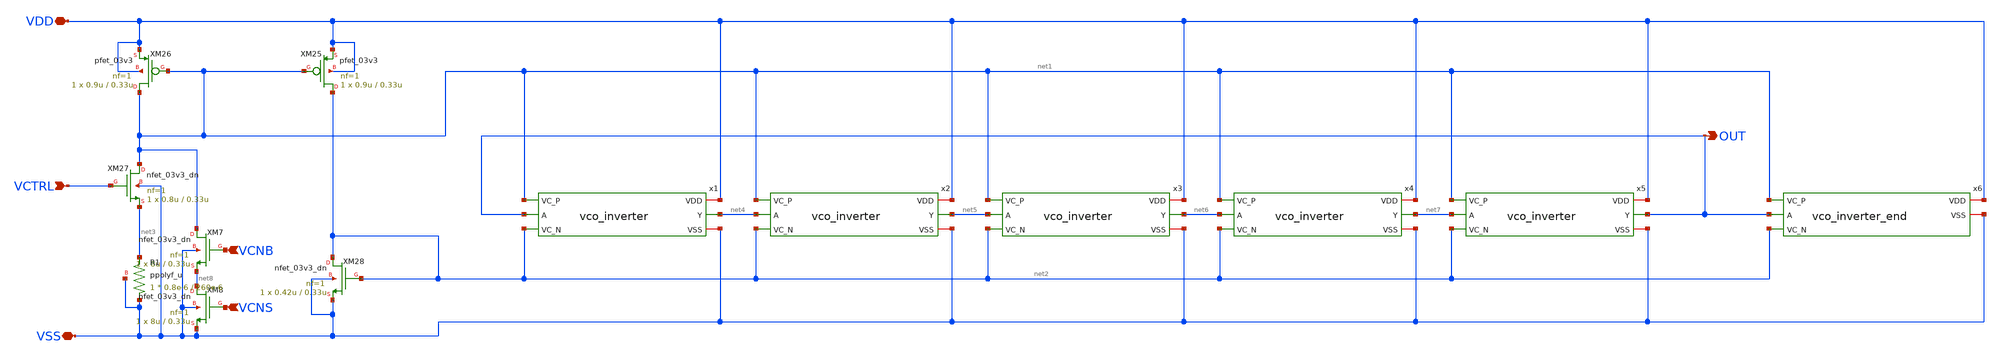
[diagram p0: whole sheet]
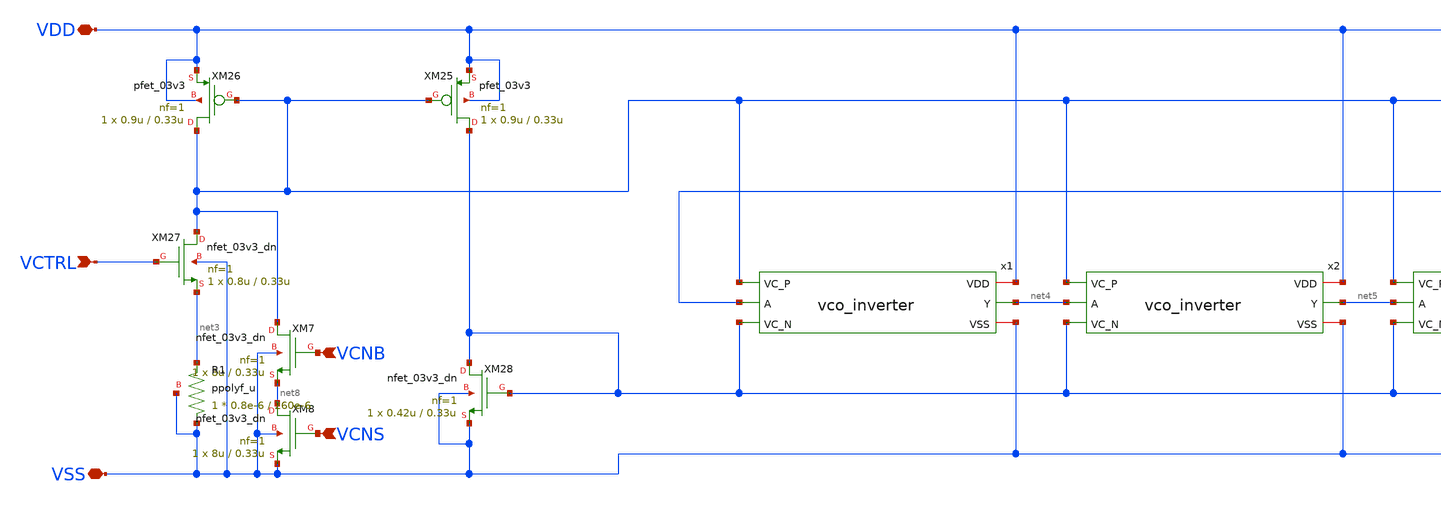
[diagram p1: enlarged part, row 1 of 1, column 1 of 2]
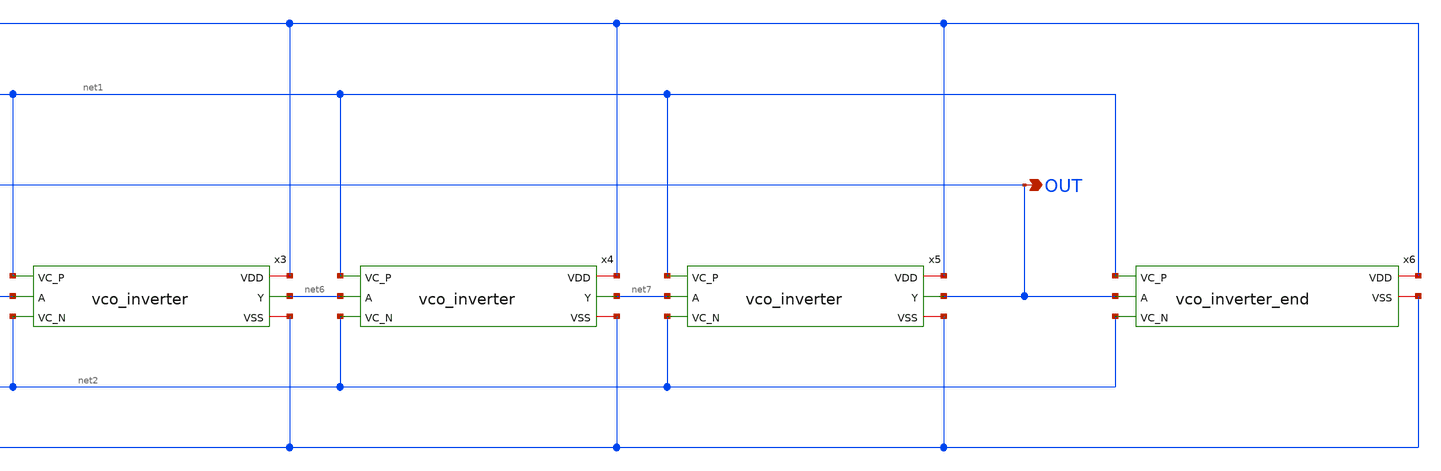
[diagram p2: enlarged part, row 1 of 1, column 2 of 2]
** sch_path: vco.sch
**.subckt vco OUT VCTRL VCNB VCNS VDD VSS
*.opin OUT
*.ipin VCTRL
*.ipin VCNB
*.ipin VCNS
*.iopin VDD
*.iopin VSS
XM25 net2 net1 VDD VDD pfet_03v3 L=0.33u W=0.9u nf=1 ad='int((nf+1)/2) * W/nf * 0.18u' as='int((nf+2)/2) * W/nf * 0.18u'
+ pd='2*int((nf+1)/2) * (W/nf + 0.18u)' ps='2*int((nf+2)/2) * (W/nf + 0.18u)' nrd='0.18u / W' nrs='0.18u / W'
+ sa=0 sb=0 sd=0 m=1
XM26 net1 net1 VDD VDD pfet_03v3 L=0.33u W=0.9u nf=1 ad='int((nf+1)/2) * W/nf * 0.18u' as='int((nf+2)/2) * W/nf * 0.18u'
+ pd='2*int((nf+1)/2) * (W/nf + 0.18u)' ps='2*int((nf+2)/2) * (W/nf + 0.18u)' nrd='0.18u / W' nrs='0.18u / W'
+ sa=0 sb=0 sd=0 m=1
XM27 net1 VCTRL net3 VSS nfet_03v3_dn L=0.33u W=0.8u nf=1 ad='int((nf+1)/2) * W/nf * 0.18u' as='int((nf+2)/2) * W/nf * 0.18u'
+ pd='2*int((nf+1)/2) * (W/nf + 0.18u)' ps='2*int((nf+2)/2) * (W/nf + 0.18u)' nrd='0.18u / W' nrs='0.18u / W'
+ sa=0 sb=0 sd=0 m=1
XM28 net2 net2 VSS VSS nfet_03v3_dn L=0.33u W=0.42u nf=1 ad='int((nf+1)/2) * W/nf * 0.18u' as='int((nf+2)/2) * W/nf * 0.18u'
+ pd='2*int((nf+1)/2) * (W/nf + 0.18u)' ps='2*int((nf+2)/2) * (W/nf + 0.18u)' nrd='0.18u / W' nrs='0.18u / W'
+ sa=0 sb=0 sd=0 m=1
x1 VDD net1 OUT net4 net2 VSS vco_inverter
x2 VDD net1 net4 net5 net2 VSS vco_inverter
x3 VDD net1 net5 net6 net2 VSS vco_inverter
x4 VDD net1 net6 net7 net2 VSS vco_inverter
x5 VDD net1 net7 OUT net2 VSS vco_inverter
x6 VDD net1 OUT net2 VSS vco_inverter_end
XM7 net1 VCNB net8 VSS nfet_03v3_dn L=0.33u W=8u nf=1 ad='int((nf+1)/2) * W/nf * 0.18u' as='int((nf+2)/2) * W/nf * 0.18u'
+ pd='2*int((nf+1)/2) * (W/nf + 0.18u)' ps='2*int((nf+2)/2) * (W/nf + 0.18u)' nrd='0.18u / W' nrs='0.18u / W'
+ sa=0 sb=0 sd=0 m=1
XM8 net8 VCNS VSS VSS nfet_03v3_dn L=0.33u W=8u nf=1 ad='int((nf+1)/2) * W/nf * 0.18u' as='int((nf+2)/2) * W/nf * 0.18u'
+ pd='2*int((nf+1)/2) * (W/nf + 0.18u)' ps='2*int((nf+2)/2) * (W/nf + 0.18u)' nrd='0.18u / W' nrs='0.18u / W'
+ sa=0 sb=0 sd=0 m=1
XR1 VSS net3 VSS ppolyf_u r_width=0.8e-6 r_length=260e-6 m=1
**.ends
.end
